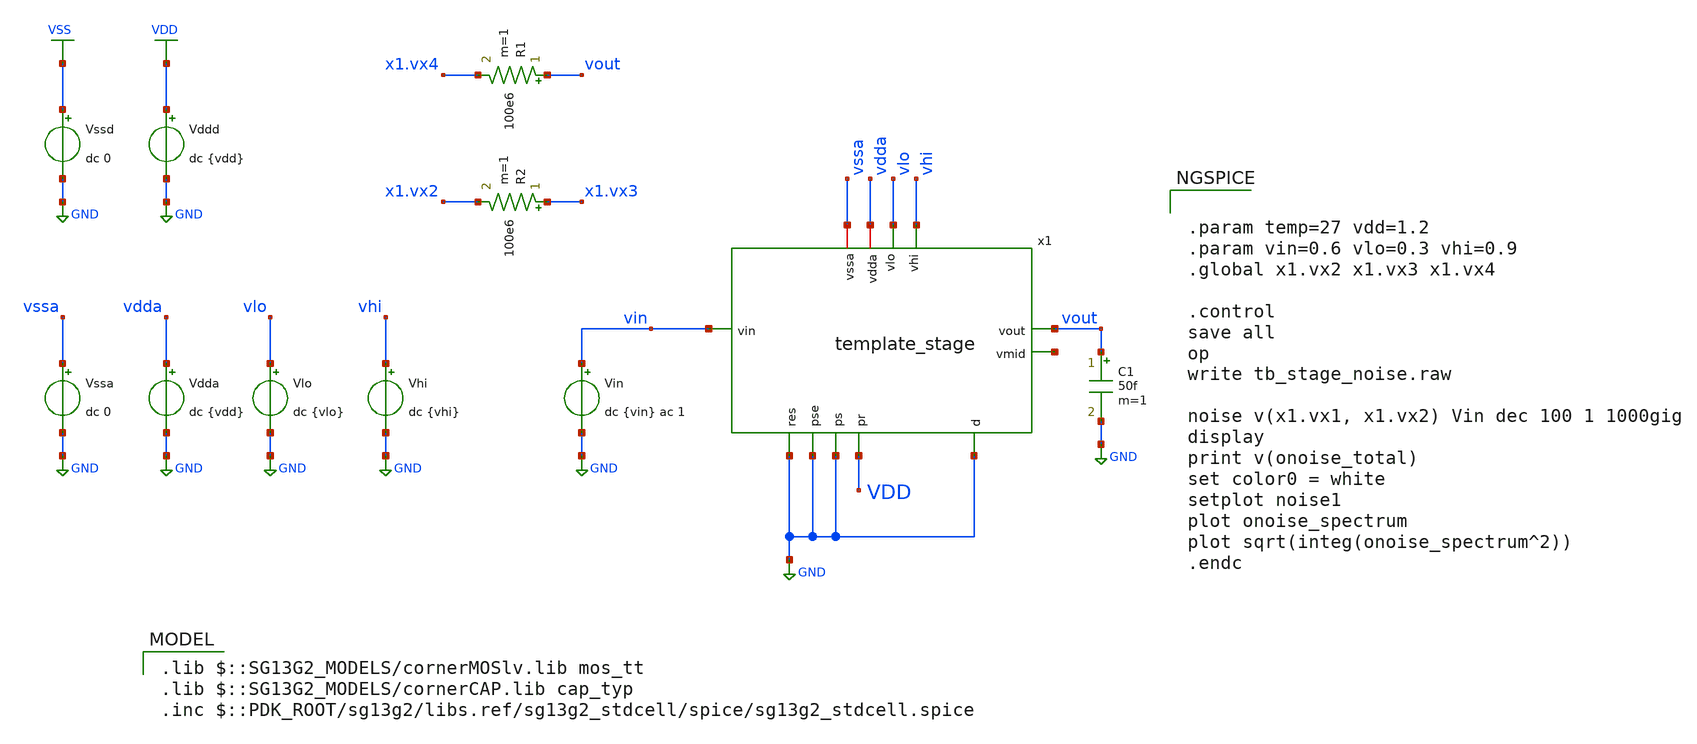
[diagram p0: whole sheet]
** sch_path: 5_Design/3_Real_circuits/sandbox_boris/tb_stage_noise.sch
* IHP-GmbH/IHP-Open-PDK/ihp-sg13g2/libs.tech/xschem/sg13g2_stdcells/sg13g2_nand2b_1.sch:
* Copyright 2023 IHP PDK Authors
* Licensed under the Apache License, Version 2.0 (the "License");
**.subckt tb_stage_noise
Vin vin GND dc {vin} ac 1
Vssa vssa GND dc 0
x1 GND GND GND VDD vhi vdda vout vin vssa GND vlo net1 template_stage
Vddd VDD GND dc {vdd}
Vssd VSS GND dc 0
Vdda vdda GND dc {vdd}
Vlo vlo GND dc {vlo}
Vhi vhi GND dc {vhi}
C1 vout GND 50f m=1
R1 vout x1.vx4 100e6 m=1
R2 x1.vx3 x1.vx2 100e6 m=1
**** begin user architecture code


.param temp=27 vdd=1.2
.param vin=0.6 vlo=0.3 vhi=0.9
.global x1.vx2 x1.vx3 x1.vx4

.control
save all
op
write tb_stage_noise.raw

noise v(x1.vx1, x1.vx2) Vin dec 100 1 1000gig
display
print v(onoise_total)
set color0 = white
setplot noise1
plot onoise_spectrum
plot sqrt(integ(onoise_spectrum^2))
.endc


 .lib $::SG13G2_MODELS/cornerMOSlv.lib mos_tt
.lib $::SG13G2_MODELS/cornerCAP.lib cap_typ
.inc $::PDK_ROOT/sg13g2/libs.ref/sg13g2_stdcell/spice/sg13g2_stdcell.spice

**** end user architecture code
**.ends

* expanding   symbol:  ../template_stage.sym # of pins=12
** sym_path: 5_Design/3_Real_circuits/template_stage.sym
** sch_path: 5_Design/3_Real_circuits/template_stage.sch
.subckt template_stage res pse ps pr vhi vdda vout vin vssa d vlo vmid
*.opin vout
*.iopin vdda
*.ipin res
*.ipin vin
*.ipin pse
*.ipin ps
*.ipin pr
*.ipin d
*.iopin vssa
*.iopin vhi
*.iopin vlo
*.opin vmid
XMn vout vx3 vssa vssa sg13_lv_nmos w=2.5u l=1.5u ng=1 m=1 mm_ok=1
XMp vout vx3 vdda vdda sg13_lv_pmos w=10u l=1.5u ng=4 m=1 mm_ok=1
XMn3 vx1 gn vlo vssa sg13_lv_nmos w=0.5u l=0.13u ng=1 m=1 mm_ok=1
XMn4 vout res vx4 vssa sg13_lv_nmos w=2u l=0.13u ng=1 m=1 mm_ok=1
x1 psb ps VDD VSS sg13g2_inv_1
XMp1 vx1 psb vin vdda sg13_lv_pmos w=6u l=0.13u ng=3 m=1 mm_ok=1
XMn5 vin ps vx1 vssa sg13_lv_nmos w=2u l=0.13u ng=1 m=1 mm_ok=1
XMn1 vx4 pr vx2 vssa sg13_lv_nmos w=2u l=0.13u ng=1 m=1 mm_ok=1
XMn2 vx4 ps vx3 vssa sg13_lv_nmos w=2u l=0.13u ng=1 m=1 mm_ok=1
XMn7 vmid vmid vssa vssa sg13_lv_nmos w=2.5u l=1.5u ng=1 m=1 mm_ok=1
XMp2 vmid vmid vdda vdda sg13_lv_pmos w=10u l=1.5u ng=4 m=1 mm_ok=1
x2 gn pr d VDD VSS sg13g2_and2_1
XMp3 vx1 gp vhi vdda sg13_lv_pmos w=1.5u l=0.13u ng=1 m=1 mm_ok=1
x3 gp d pr VDD VSS sg13g2_nand2b_1
XC1 vx2 vx1 cap_cmim w=5.77e-6 l=5.77e-6 m=1 mm_ok=1
XC2 vx3 vx2 cap_cmim w=8.16e-6 l=8.16e-6 m=1 mm_ok=1
XC3 vx4 vout cap_cmim w=8.16e-6 l=8.16e-6 m=1 mm_ok=1
XMn6 vx2 pse vmid vssa sg13_lv_nmos w=2u l=0.13u ng=1 m=1 mm_ok=1
.ends


* expanding   symbol:  sg13g2_stdcells/sg13g2_inv_1.sym # of pins=2
** sym_path: sg13g2_stdcells/sg13g2_inv_1.sym
** sch_path: sg13g2_stdcells/sg13g2_inv_1.sch
.subckt sg13g2_inv_1 Y A VDD VSS
*.opin Y
*.ipin A
*.iopin VDD
*.iopin VSS
XM1 Y A VSS VSS sg13_lv_nmos w=740.00n l=130.00n ng=1 m=1 mm_ok=1
XM2 Y A VDD VDD sg13_lv_pmos w=1.12u l=130.00n ng=1 m=1 mm_ok=1
.ends


* expanding   symbol:  sg13g2_stdcells/sg13g2_and2_1.sym # of pins=3
** sym_path: sg13g2_stdcells/sg13g2_and2_1.sym
** sch_path: sg13g2_stdcells/sg13g2_and2_1.sch
.subckt sg13g2_and2_1 X A B VDD VSS
*.ipin A
*.ipin B
*.opin X
*.iopin VDD
*.iopin VSS
XM1 net1 A net2 VSS sg13_lv_nmos w=640.00n l=130.00n ng=1 m=1 mm_ok=1
XM2 net2 B VSS VSS sg13_lv_nmos w=640.00n l=130.00n ng=1 m=1 mm_ok=1
XM3 X net1 VSS VSS sg13_lv_nmos w=740.00n l=130.00n ng=1 m=1 mm_ok=1
XM4 net1 B VDD VDD sg13_lv_pmos w=840.00n l=130.00n ng=1 m=1 mm_ok=1
XM5 net1 A VDD VDD sg13_lv_pmos w=840.00n l=130.00n ng=1 m=1 mm_ok=1
XM6 X net1 VDD VDD sg13_lv_pmos w=1.12u l=130.00n ng=1 m=1 mm_ok=1
.ends


* expanding   symbol:  sg13g2_stdcells/sg13g2_nand2b_1.sym # of pins=3
** sym_path: sg13g2_stdcells/sg13g2_nand2b_1.sym
** sch_path: sg13g2_stdcells/sg13g2_nand2b_1.sch
.subckt sg13g2_nand2b_1 Y A_N B VDD VSS
*.opin Y
*.ipin B
*.ipin A_N
*.iopin VDD
*.iopin VSS
XM1 net1 A_N VSS VSS sg13_lv_nmos w=550.00n l=130.00n ng=1 m=1 mm_ok=1
XM2 Y net1 net2 VSS sg13_lv_nmos w=740.00n l=130.00n ng=1 m=1 mm_ok=1
XM3 net2 B VSS VSS sg13_lv_nmos w=740.00n l=130.00n ng=1 m=1 mm_ok=1
XM4 Y B VDD VDD sg13_lv_pmos w=1.12u l=130.00n ng=1 m=1 mm_ok=1
XM5 net1 A_N VDD VDD sg13_lv_pmos w=840.00n l=130.00n ng=1 m=1 mm_ok=1
XM6 Y net1 VDD VDD sg13_lv_pmos w=1.12u l=130.00n ng=1 m=1 mm_ok=1
.ends

.GLOBAL GND
.GLOBAL VDD
.GLOBAL VSS
.end
